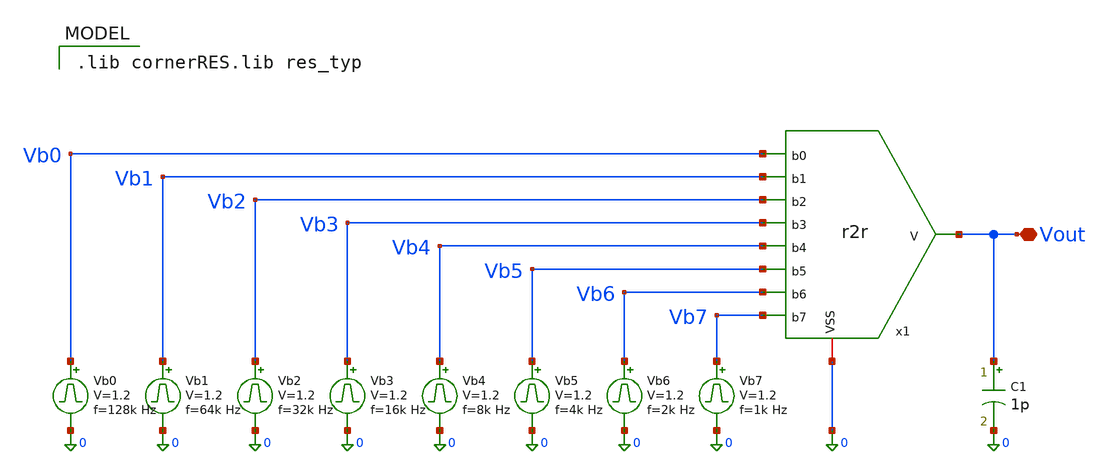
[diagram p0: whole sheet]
** sch_path: xschem/r2r_tb.sch
**.subckt r2r_tb Vout
*.iopin Vout
C1 Vout 0 1p m=1
x1 Vb3 Vb1 Vb2 Vb0 Vb4 Vb5 Vb6 Vb7 Vout 0 r2r
Vb7 Vb7 0 pulse 0 1.2 '0.495/ 1k ' '0.01/1k ' '0.01/1k ' '0.49/1k ' '1/1k '
Vb6 Vb6 0 pulse 0 1.2 '0.495/ 2k ' '0.01/2k ' '0.01/2k ' '0.49/2k ' '1/2k '
Vb5 Vb5 0 pulse 0 1.2 '0.495/ 4k ' '0.01/4k ' '0.01/4k ' '0.49/4k ' '1/4k '
Vb4 Vb4 0 pulse 0 1.2 '0.495/ 8k ' '0.01/8k ' '0.01/8k ' '0.49/8k ' '1/8k '
Vb3 Vb3 0 pulse 0 1.2 '0.495/ 16k ' '0.01/16k ' '0.01/16k ' '0.49/16k ' '1/16k '
Vb2 Vb2 0 pulse 0 1.2 '0.495/ 32k ' '0.01/32k ' '0.01/32k ' '0.49/32k ' '1/32k '
Vb1 Vb1 0 pulse 0 1.2 '0.495/ 64k ' '0.01/64k ' '0.01/64k ' '0.49/64k ' '1/64k '
Vb0 Vb0 0 pulse 0 1.2 '0.495/ 128k ' '0.01/128k ' '0.01/128k ' '0.49/128k ' '1/128k '
**** begin user architecture code
 .lib cornerRES.lib res_typ



.param temp=27
.option method=gear
.control
op
write r2r_tb.raw
set appendwrite
reset
save all
tran 1us 1.1ms
write r2r_tb.raw
quit 0
.endc


**** end user architecture code
**.ends

* expanding   symbol:  r2r.sym # of pins=10
** sym_path: xschem/r2r.sym
** sch_path: xschem/r2r.sch
.subckt r2r b3 b1 b2 b0 b4 b5 b6 b7 V VSS
*.iopin VSS
*.ipin b0
*.ipin b1
*.ipin b2
*.ipin b3
*.ipin b4
*.ipin b5
*.ipin b6
*.ipin b7
*.opin V
XR1 net1 VSS sub! rsil w=.5u l=.5u m=1 mm_ok=1
XR2 b0 net1 sub! rsil w=.5u l=.5u m=1 mm_ok=1
XR3 net2 net1 sub! rsil w=1u l=.5u m=1 mm_ok=1
XR4 b1 net2 sub! rsil w=.5u l=.5u m=1 mm_ok=1
XR5 net3 net2 sub! rsil w=1u l=.5u m=1 mm_ok=1
XR6 b2 net3 sub! rsil w=.5u l=.5u m=1 mm_ok=1
XR7 net4 net3 sub! rsil w=1u l=.5u m=1 mm_ok=1
XR8 b3 net4 sub! rsil w=.5u l=.5u m=1 mm_ok=1
XR9 net5 net4 sub! rsil w=1u l=.5u m=1 mm_ok=1
XR10 b4 net5 sub! rsil w=.5u l=.5u m=1 mm_ok=1
XR11 net6 net5 sub! rsil w=1u l=.5u m=1 mm_ok=1
XR12 b5 net6 sub! rsil w=.5u l=.5u m=1 mm_ok=1
XR13 net7 net6 sub! rsil w=1u l=.5u m=1 mm_ok=1
XR14 b6 net7 sub! rsil w=.5u l=.5u m=1 mm_ok=1
XR15 net8 net7 sub! rsil w=1u l=.5u m=1 mm_ok=1
XR16 b7 net8 sub! rsil w=.5u l=.5u m=1 mm_ok=1
XR17 V net8 sub! rsil w=1u l=.5u m=1 mm_ok=1
.ends

.end
